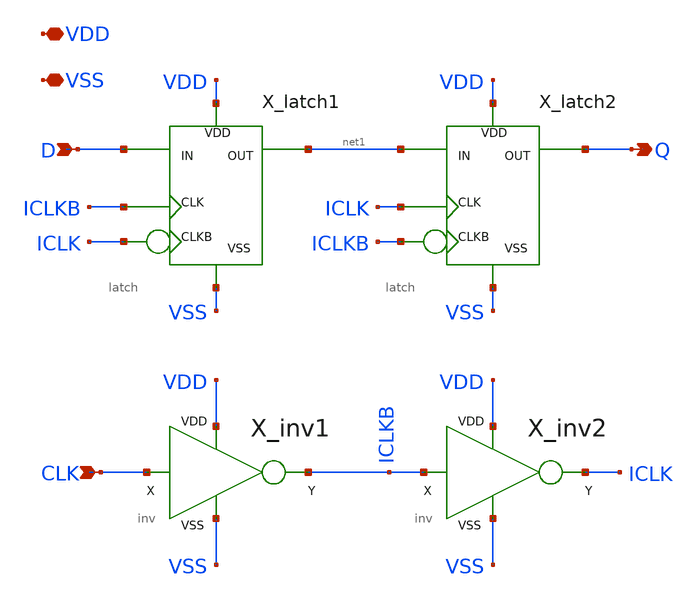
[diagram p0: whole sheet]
** sch_path: xschem_example/DFF_tinv.sch
**.subckt DFF_tinv D CLK VSS VDD Q
*.ipin D
*.ipin CLK
*.iopin VSS
*.iopin VDD
*.opin Q
X_latch1 D ICLKB ICLK VSS VDD net1 latch
X_latch2 net1 ICLK ICLKB VSS VDD Q latch
X_inv1 CLK VDD VSS ICLKB inv
X_inv2 ICLKB VDD VSS ICLK inv
**.ends

* expanding   symbol:  xschem_example/latch.sym # of pins=6
** sym_path: xschem_example/latch.sym
** sch_path: xschem_example/latch.sch
.subckt latch IN CLK CLKB VSS VDD OUT
*.ipin CLKB
*.ipin IN
*.ipin CLK
*.iopin VDD
*.iopin VSS
*.opin OUT
X_inv1 net1 VDD VSS OUT inv
X_tinv1 IN CLK CLKB VDD VSS net1 tinv
X_tinv_small1 OUT CLKB CLK VDD VSS net1 tinv_small
.ends


* expanding   symbol:  xschem_example/inv.sym # of pins=4
** sym_path: xschem_example/inv.sym
** sch_path: xschem_example/inv.sch
.subckt inv X VDD VSS Y
*.iopin VSS
*.ipin X
*.opin Y
*.iopin VDD
XM1 Y X VSS VSS sky130_fd_pr__nfet_01v8_lvt L=0.15 W=1.2 nf=1 ad='int((nf+1)/2) * W/nf * 0.29' as='int((nf+2)/2) * W/nf * 0.29'
+ pd='2*int((nf+1)/2) * (W/nf + 0.29)' ps='2*int((nf+2)/2) * (W/nf + 0.29)' nrd='0.29 / W' nrs='0.29 / W'
+ sa=0 sb=0 sd=0 mult=8 m=8
XM2 Y X VDD VDD sky130_fd_pr__pfet_01v8 L=0.15 W=1.6 nf=1 ad='int((nf+1)/2) * W/nf * 0.29' as='int((nf+2)/2) * W/nf * 0.29'
+ pd='2*int((nf+1)/2) * (W/nf + 0.29)' ps='2*int((nf+2)/2) * (W/nf + 0.29)' nrd='0.29 / W' nrs='0.29 / W'
+ sa=0 sb=0 sd=0 mult=8 m=8
.ends


* expanding   symbol:  xschem_example/tinv.sym # of pins=6
** sym_path: xschem_example/tinv.sym
** sch_path: xschem_example/tinv.sch
.subckt tinv X EN ENB VDD VSS Y
*.ipin X
*.ipin ENB
*.ipin EN
*.opin Y
*.iopin VDD
*.iopin VSS
XM1 net2 X VDD VDD sky130_fd_pr__pfet_01v8 L=0.15 W=1.6 nf=1 ad='int((nf+1)/2) * W/nf * 0.29' as='int((nf+2)/2) * W/nf * 0.29'
+ pd='2*int((nf+1)/2) * (W/nf + 0.29)' ps='2*int((nf+2)/2) * (W/nf + 0.29)' nrd='0.29 / W' nrs='0.29 / W'
+ sa=0 sb=0 sd=0 mult=4 m=4
XM2 Y ENB net2 VDD sky130_fd_pr__pfet_01v8 L=0.15 W=1.6 nf=1 ad='int((nf+1)/2) * W/nf * 0.29' as='int((nf+2)/2) * W/nf * 0.29'
+ pd='2*int((nf+1)/2) * (W/nf + 0.29)' ps='2*int((nf+2)/2) * (W/nf + 0.29)' nrd='0.29 / W' nrs='0.29 / W'
+ sa=0 sb=0 sd=0 mult=4 m=4
XM3 Y EN net1 VSS sky130_fd_pr__nfet_01v8_lvt L=0.15 W=1.2 nf=1 ad='int((nf+1)/2) * W/nf * 0.29' as='int((nf+2)/2) * W/nf * 0.29'
+ pd='2*int((nf+1)/2) * (W/nf + 0.29)' ps='2*int((nf+2)/2) * (W/nf + 0.29)' nrd='0.29 / W' nrs='0.29 / W'
+ sa=0 sb=0 sd=0 mult=4 m=4
XM4 net1 X VSS VSS sky130_fd_pr__nfet_01v8_lvt L=0.15 W=1.2 nf=1 ad='int((nf+1)/2) * W/nf * 0.29' as='int((nf+2)/2) * W/nf * 0.29'
+ pd='2*int((nf+1)/2) * (W/nf + 0.29)' ps='2*int((nf+2)/2) * (W/nf + 0.29)' nrd='0.29 / W' nrs='0.29 / W'
+ sa=0 sb=0 sd=0 mult=4 m=4
.ends


* expanding   symbol:  xschem_example/tinv_small.sym # of pins=6
** sym_path: xschem_lib/sylee21/tinv_small.sym
** sch_path: xschem_lib/sylee21/tinv_small.sch
.subckt tinv_small X EN ENB VDD VSS Y
*.ipin X
*.ipin ENB
*.ipin EN
*.opin Y
*.iopin VDD
*.iopin VSS
XM1 net2 X VDD VDD sky130_fd_pr__pfet_01v8 L=0.15 W=2.4 nf=1 ad='int((nf+1)/2) * W/nf * 0.29' as='int((nf+2)/2) * W/nf * 0.29'
+ pd='2*int((nf+1)/2) * (W/nf + 0.29)' ps='2*int((nf+2)/2) * (W/nf + 0.29)' nrd='0.29 / W' nrs='0.29 / W'
+ sa=0 sb=0 sd=0 mult=1 m=1
XM2 Y ENB net2 VDD sky130_fd_pr__pfet_01v8 L=0.15 W=2.4 nf=1 ad='int((nf+1)/2) * W/nf * 0.29' as='int((nf+2)/2) * W/nf * 0.29'
+ pd='2*int((nf+1)/2) * (W/nf + 0.29)' ps='2*int((nf+2)/2) * (W/nf + 0.29)' nrd='0.29 / W' nrs='0.29 / W'
+ sa=0 sb=0 sd=0 mult=1 m=1
XM3 Y EN net1 VSS sky130_fd_pr__nfet_01v8_lvt L=0.15 W=1.2 nf=1 ad='int((nf+1)/2) * W/nf * 0.29' as='int((nf+2)/2) * W/nf * 0.29'
+ pd='2*int((nf+1)/2) * (W/nf + 0.29)' ps='2*int((nf+2)/2) * (W/nf + 0.29)' nrd='0.29 / W' nrs='0.29 / W'
+ sa=0 sb=0 sd=0 mult=1 m=1
XM4 net1 X VSS VSS sky130_fd_pr__nfet_01v8_lvt L=0.15 W=1.2 nf=1 ad='int((nf+1)/2) * W/nf * 0.29' as='int((nf+2)/2) * W/nf * 0.29'
+ pd='2*int((nf+1)/2) * (W/nf + 0.29)' ps='2*int((nf+2)/2) * (W/nf + 0.29)' nrd='0.29 / W' nrs='0.29 / W'
+ sa=0 sb=0 sd=0 mult=1 m=1
.ends

.end
